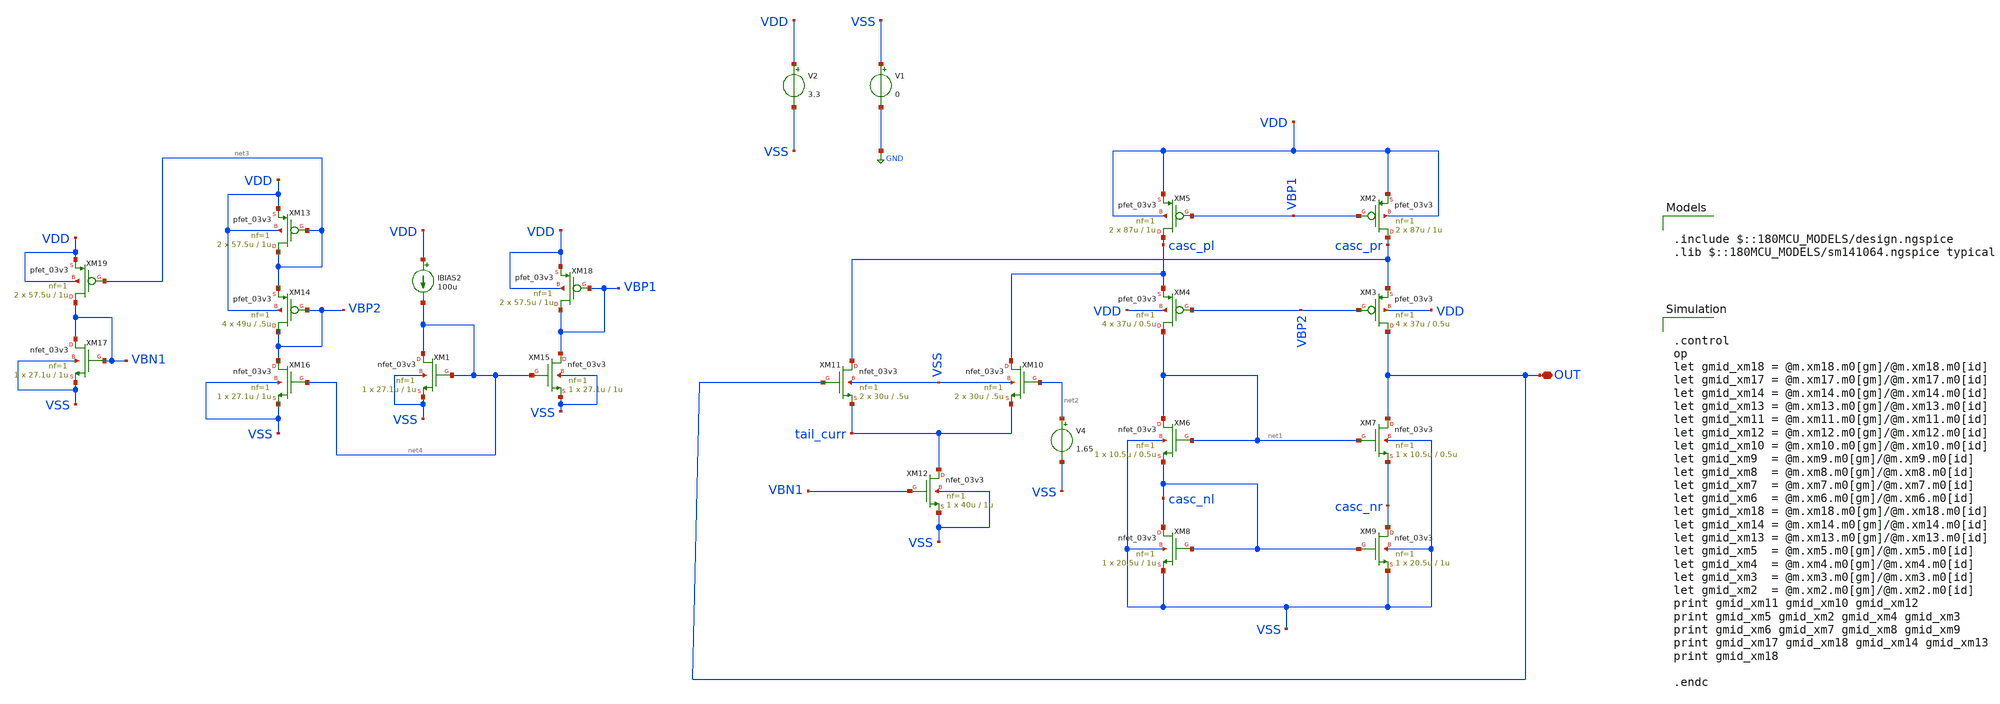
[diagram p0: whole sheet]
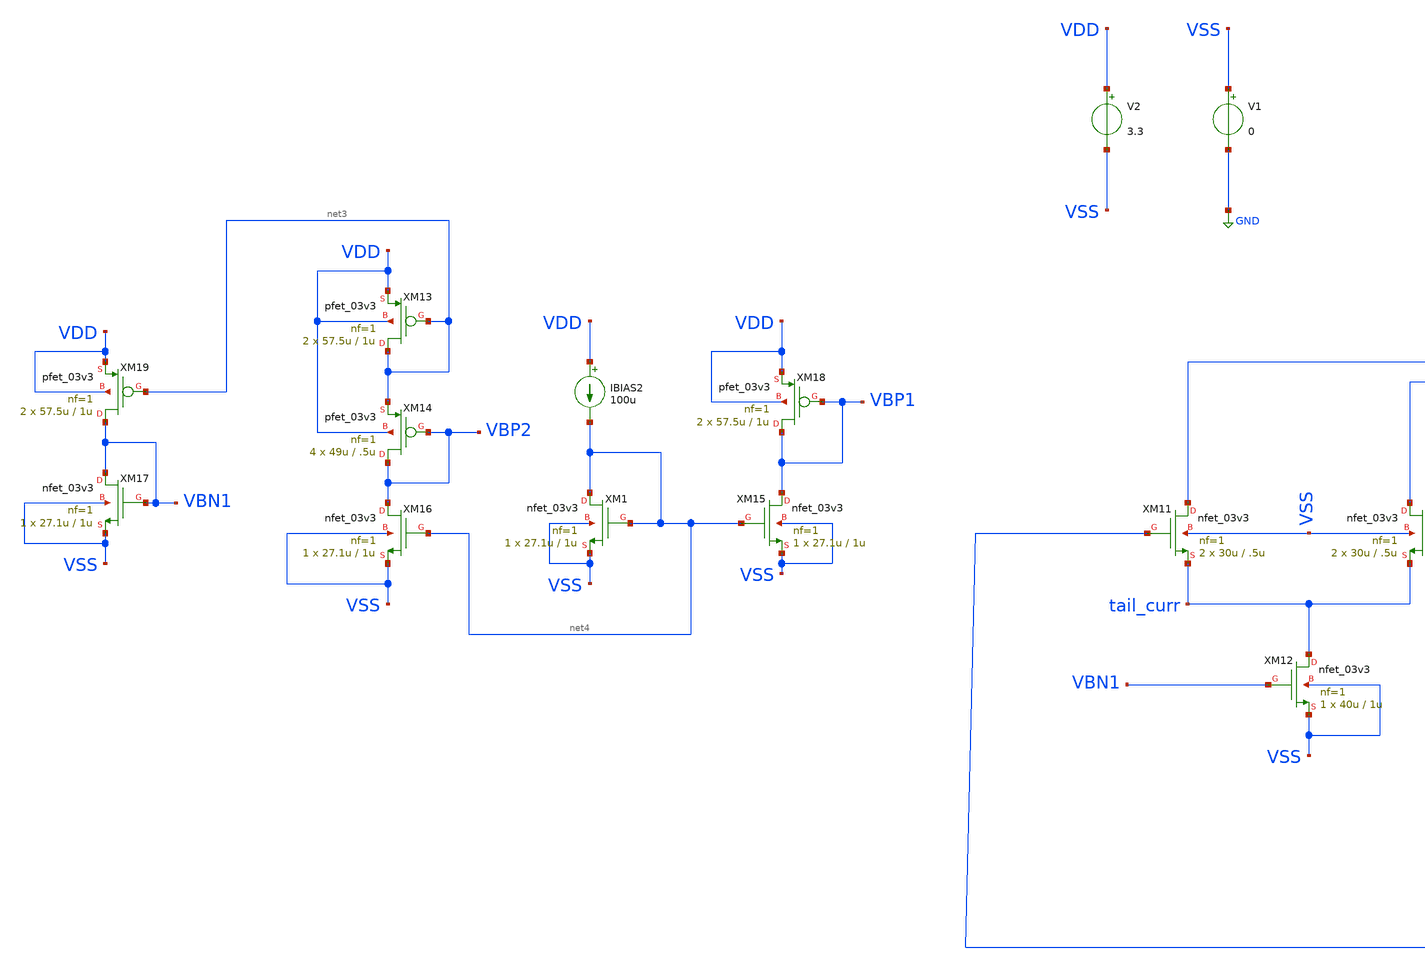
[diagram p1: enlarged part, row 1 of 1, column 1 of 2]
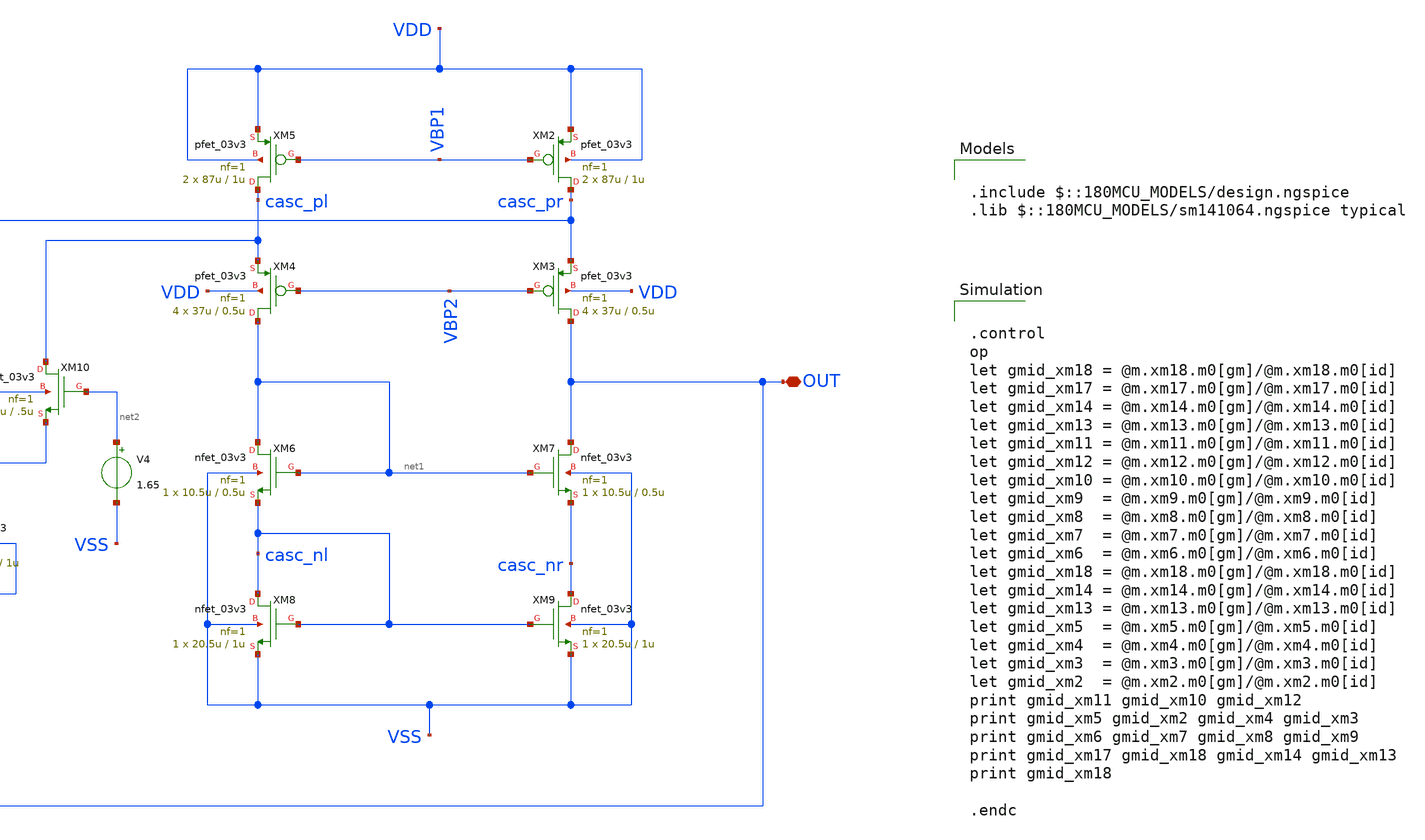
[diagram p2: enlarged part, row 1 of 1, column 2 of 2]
** sch_path: designs/libs/old_files/old_amps/ota_folded_cascode/etj_folded_new.sch
**.subckt etj_folded_new OUT
*.iopin OUT
XM2 casc_pr VBP1 VDD VDD pfet_03v3 L=1u W=87u nf=1 ad='int((nf+1)/2) * W/nf * 0.18u' as='int((nf+2)/2) * W/nf * 0.18u'
+ pd='2*int((nf+1)/2) * (W/nf + 0.18u)' ps='2*int((nf+2)/2) * (W/nf + 0.18u)' nrd='0.18u / W' nrs='0.18u / W'
+ sa=0 sb=0 sd=0 m=2
XM3 OUT VBP2 casc_pr VDD pfet_03v3 L=0.5u W=37u nf=1 ad='int((nf+1)/2) * W/nf * 0.18u' as='int((nf+2)/2) * W/nf * 0.18u'
+ pd='2*int((nf+1)/2) * (W/nf + 0.18u)' ps='2*int((nf+2)/2) * (W/nf + 0.18u)' nrd='0.18u / W' nrs='0.18u / W'
+ sa=0 sb=0 sd=0 m=4
XM4 net1 VBP2 casc_pl VDD pfet_03v3 L=0.5u W=37u nf=1 ad='int((nf+1)/2) * W/nf * 0.18u' as='int((nf+2)/2) * W/nf * 0.18u'
+ pd='2*int((nf+1)/2) * (W/nf + 0.18u)' ps='2*int((nf+2)/2) * (W/nf + 0.18u)' nrd='0.18u / W' nrs='0.18u / W'
+ sa=0 sb=0 sd=0 m=4
XM5 casc_pl VBP1 VDD VDD pfet_03v3 L=1u W=87u nf=1 ad='int((nf+1)/2) * W/nf * 0.18u' as='int((nf+2)/2) * W/nf * 0.18u'
+ pd='2*int((nf+1)/2) * (W/nf + 0.18u)' ps='2*int((nf+2)/2) * (W/nf + 0.18u)' nrd='0.18u / W' nrs='0.18u / W'
+ sa=0 sb=0 sd=0 m=2
XM6 net1 net1 casc_nl VSS nfet_03v3 L=0.5u W=10.5u nf=1 ad='int((nf+1)/2) * W/nf * 0.18u' as='int((nf+2)/2) * W/nf * 0.18u'
+ pd='2*int((nf+1)/2) * (W/nf + 0.18u)' ps='2*int((nf+2)/2) * (W/nf + 0.18u)' nrd='0.18u / W' nrs='0.18u / W'
+ sa=0 sb=0 sd=0 m=1
XM7 OUT net1 casc_nr VSS nfet_03v3 L=0.5u W=10.5u nf=1 ad='int((nf+1)/2) * W/nf * 0.18u' as='int((nf+2)/2) * W/nf * 0.18u'
+ pd='2*int((nf+1)/2) * (W/nf + 0.18u)' ps='2*int((nf+2)/2) * (W/nf + 0.18u)' nrd='0.18u / W' nrs='0.18u / W'
+ sa=0 sb=0 sd=0 m=1
XM8 casc_nl casc_nl VSS VSS nfet_03v3 L=1u W=20.5u nf=1 ad='int((nf+1)/2) * W/nf * 0.18u' as='int((nf+2)/2) * W/nf * 0.18u'
+ pd='2*int((nf+1)/2) * (W/nf + 0.18u)' ps='2*int((nf+2)/2) * (W/nf + 0.18u)' nrd='0.18u / W' nrs='0.18u / W'
+ sa=0 sb=0 sd=0 m=1
XM9 casc_nr casc_nl VSS VSS nfet_03v3 L=1u W=20.5u nf=1 ad='int((nf+1)/2) * W/nf * 0.18u' as='int((nf+2)/2) * W/nf * 0.18u'
+ pd='2*int((nf+1)/2) * (W/nf + 0.18u)' ps='2*int((nf+2)/2) * (W/nf + 0.18u)' nrd='0.18u / W' nrs='0.18u / W'
+ sa=0 sb=0 sd=0 m=1
XM10 casc_pl net2 tail_curr VSS nfet_03v3 L=.5u W=30u nf=1 ad='int((nf+1)/2) * W/nf * 0.18u' as='int((nf+2)/2) * W/nf * 0.18u'
+ pd='2*int((nf+1)/2) * (W/nf + 0.18u)' ps='2*int((nf+2)/2) * (W/nf + 0.18u)' nrd='0.18u / W' nrs='0.18u / W'
+ sa=0 sb=0 sd=0 m=2
XM12 tail_curr VBN1 VSS VSS nfet_03v3 L=1u W=40u nf=1 ad='int((nf+1)/2) * W/nf * 0.18u' as='int((nf+2)/2) * W/nf * 0.18u'
+ pd='2*int((nf+1)/2) * (W/nf + 0.18u)' ps='2*int((nf+2)/2) * (W/nf + 0.18u)' nrd='0.18u / W' nrs='0.18u / W'
+ sa=0 sb=0 sd=0 m=1
XM11 casc_pr OUT tail_curr VSS nfet_03v3 L=.5u W=30u nf=1 ad='int((nf+1)/2) * W/nf * 0.18u' as='int((nf+2)/2) * W/nf * 0.18u'
+ pd='2*int((nf+1)/2) * (W/nf + 0.18u)' ps='2*int((nf+2)/2) * (W/nf + 0.18u)' nrd='0.18u / W' nrs='0.18u / W'
+ sa=0 sb=0 sd=0 m=2
V2 VDD VSS 3.3
V1 VSS GND 0
V4 net2 VSS 1.65
XM13 net3 net3 VDD VDD pfet_03v3 L=1u W=57.5u nf=1 ad='int((nf+1)/2) * W/nf * 0.18u' as='int((nf+2)/2) * W/nf * 0.18u'
+ pd='2*int((nf+1)/2) * (W/nf + 0.18u)' ps='2*int((nf+2)/2) * (W/nf + 0.18u)' nrd='0.18u / W' nrs='0.18u / W'
+ sa=0 sb=0 sd=0 m=2
XM14 VBP2 VBP2 net3 VDD pfet_03v3 L=.5u W=49u nf=1 ad='int((nf+1)/2) * W/nf * 0.18u' as='int((nf+2)/2) * W/nf * 0.18u'
+ pd='2*int((nf+1)/2) * (W/nf + 0.18u)' ps='2*int((nf+2)/2) * (W/nf + 0.18u)' nrd='0.18u / W' nrs='0.18u / W'
+ sa=0 sb=0 sd=0 m=4
XM17 VBN1 VBN1 VSS VSS nfet_03v3 L=1u W=27.1u nf=1 ad='int((nf+1)/2) * W/nf * 0.18u' as='int((nf+2)/2) * W/nf * 0.18u'
+ pd='2*int((nf+1)/2) * (W/nf + 0.18u)' ps='2*int((nf+2)/2) * (W/nf + 0.18u)' nrd='0.18u / W' nrs='0.18u / W'
+ sa=0 sb=0 sd=0 m=1
XM18 VBP1 VBP1 VDD VDD pfet_03v3 L=1u W=57.5u nf=1 ad='int((nf+1)/2) * W/nf * 0.18u' as='int((nf+2)/2) * W/nf * 0.18u'
+ pd='2*int((nf+1)/2) * (W/nf + 0.18u)' ps='2*int((nf+2)/2) * (W/nf + 0.18u)' nrd='0.18u / W' nrs='0.18u / W'
+ sa=0 sb=0 sd=0 m=2
IBIAS2 VDD net4 100u
XM1 net4 net4 VSS VSS nfet_03v3 L=1u W=27.1u nf=1 ad='int((nf+1)/2) * W/nf * 0.18u' as='int((nf+2)/2) * W/nf * 0.18u'
+ pd='2*int((nf+1)/2) * (W/nf + 0.18u)' ps='2*int((nf+2)/2) * (W/nf + 0.18u)' nrd='0.18u / W' nrs='0.18u / W'
+ sa=0 sb=0 sd=0 m=1
XM15 VBP1 net4 VSS VSS nfet_03v3 L=1u W=27.1u nf=1 ad='int((nf+1)/2) * W/nf * 0.18u' as='int((nf+2)/2) * W/nf * 0.18u'
+ pd='2*int((nf+1)/2) * (W/nf + 0.18u)' ps='2*int((nf+2)/2) * (W/nf + 0.18u)' nrd='0.18u / W' nrs='0.18u / W'
+ sa=0 sb=0 sd=0 m=1
XM16 VBP2 net4 VSS VSS nfet_03v3 L=1u W=27.1u nf=1 ad='int((nf+1)/2) * W/nf * 0.18u' as='int((nf+2)/2) * W/nf * 0.18u'
+ pd='2*int((nf+1)/2) * (W/nf + 0.18u)' ps='2*int((nf+2)/2) * (W/nf + 0.18u)' nrd='0.18u / W' nrs='0.18u / W'
+ sa=0 sb=0 sd=0 m=1
XM19 VBN1 net3 VDD VDD pfet_03v3 L=1u W=57.5u nf=1 ad='int((nf+1)/2) * W/nf * 0.18u' as='int((nf+2)/2) * W/nf * 0.18u'
+ pd='2*int((nf+1)/2) * (W/nf + 0.18u)' ps='2*int((nf+2)/2) * (W/nf + 0.18u)' nrd='0.18u / W' nrs='0.18u / W'
+ sa=0 sb=0 sd=0 m=2
**** begin user architecture code

.include $::180MCU_MODELS/design.ngspice
.lib $::180MCU_MODELS/sm141064.ngspice typical



.control
op
let gmid_xm18 = @m.xm18.m0[gm]/@m.xm18.m0[id]
let gmid_xm17 = @m.xm17.m0[gm]/@m.xm17.m0[id]
let gmid_xm14 = @m.xm14.m0[gm]/@m.xm14.m0[id]
let gmid_xm13 = @m.xm13.m0[gm]/@m.xm13.m0[id]
let gmid_xm11 = @m.xm11.m0[gm]/@m.xm11.m0[id]
let gmid_xm12 = @m.xm12.m0[gm]/@m.xm12.m0[id]
let gmid_xm10 = @m.xm10.m0[gm]/@m.xm10.m0[id]
let gmid_xm9  = @m.xm9.m0[gm]/@m.xm9.m0[id]
let gmid_xm8  = @m.xm8.m0[gm]/@m.xm8.m0[id]
let gmid_xm7  = @m.xm7.m0[gm]/@m.xm7.m0[id]
let gmid_xm6  = @m.xm6.m0[gm]/@m.xm6.m0[id]
let gmid_xm18 = @m.xm18.m0[gm]/@m.xm18.m0[id]
let gmid_xm14 = @m.xm14.m0[gm]/@m.xm14.m0[id]
let gmid_xm13 = @m.xm13.m0[gm]/@m.xm13.m0[id]
let gmid_xm5  = @m.xm5.m0[gm]/@m.xm5.m0[id]
let gmid_xm4  = @m.xm4.m0[gm]/@m.xm4.m0[id]
let gmid_xm3  = @m.xm3.m0[gm]/@m.xm3.m0[id]
let gmid_xm2  = @m.xm2.m0[gm]/@m.xm2.m0[id]
print gmid_xm11 gmid_xm10 gmid_xm12
print gmid_xm5 gmid_xm2 gmid_xm4 gmid_xm3
print gmid_xm6 gmid_xm7 gmid_xm8 gmid_xm9
print gmid_xm17 gmid_xm18 gmid_xm14 gmid_xm13
print gmid_xm18

.endc


**** end user architecture code
**.ends
.GLOBAL GND
.end
